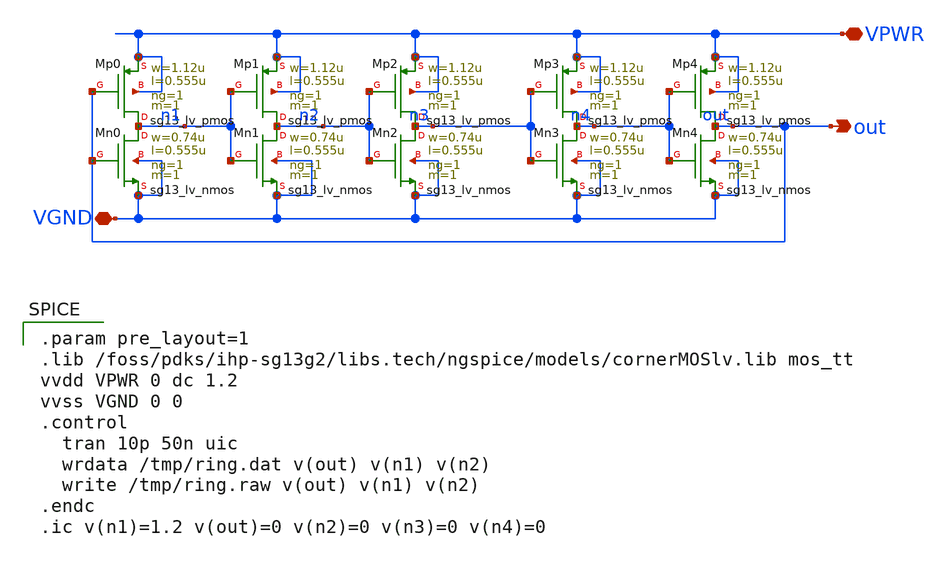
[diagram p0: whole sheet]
** sch_path: analog/transistor_ring_oscillator_500mhz/schematic/main_5.sch
**.subckt main_5 VPWR VGND out
*.iopin VPWR
*.iopin VGND
*.opin out
XMp0 n1 out VPWR VPWR sg13_lv_pmos w=1.12u l=0.555u ng=1 m=1 mm_ok=1
XMn0 n1 out VGND VGND sg13_lv_nmos w=0.74u l=0.555u ng=1 m=1 mm_ok=1
XMp1 n2 n1 VPWR VPWR sg13_lv_pmos w=1.12u l=0.555u ng=1 m=1 mm_ok=1
XMn1 n2 n1 VGND VGND sg13_lv_nmos w=0.74u l=0.555u ng=1 m=1 mm_ok=1
XMp2 n3 n2 VPWR VPWR sg13_lv_pmos w=1.12u l=0.555u ng=1 m=1 mm_ok=1
XMn2 n3 n2 VGND VGND sg13_lv_nmos w=0.74u l=0.555u ng=1 m=1 mm_ok=1
XMp3 n4 n3 VPWR VPWR sg13_lv_pmos w=1.12u l=0.555u ng=1 m=1 mm_ok=1
XMn3 n4 n3 VGND VGND sg13_lv_nmos w=0.74u l=0.555u ng=1 m=1 mm_ok=1
XMp4 out n4 VPWR VPWR sg13_lv_pmos w=1.12u l=0.555u ng=1 m=1 mm_ok=1
XMn4 out n4 VGND VGND sg13_lv_nmos w=0.74u l=0.555u ng=1 m=1 mm_ok=1
**** begin user architecture code

.param pre_layout=1
.lib /foss/pdks/ihp-sg13g2/libs.tech/ngspice/models/cornerMOSlv.lib mos_tt
vvdd VPWR 0 dc 1.2
vvss VGND 0 0
.control
  tran 10p 50n uic
  wrdata /tmp/ring.dat v(out) v(n1) v(n2)
  write /tmp/ring.raw v(out) v(n1) v(n2)
.endc
.ic v(n1)=1.2 v(out)=0 v(n2)=0 v(n3)=0 v(n4)=0


**** end user architecture code
**.ends
.end
